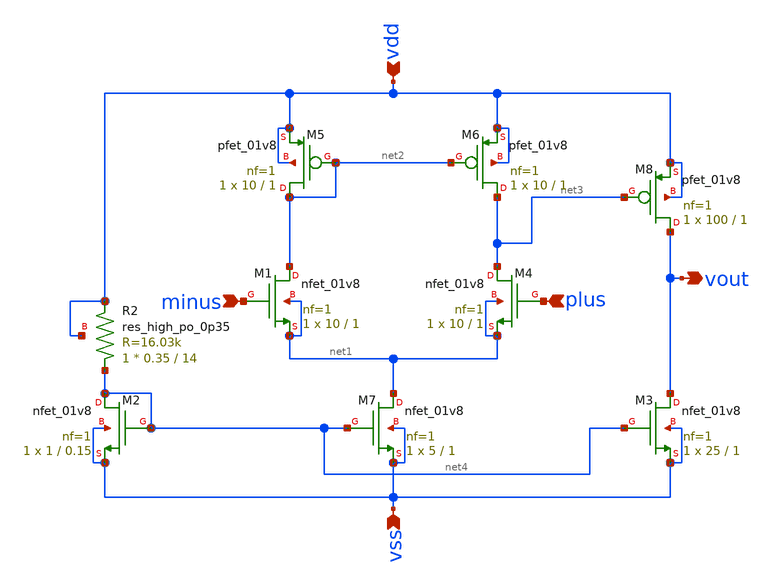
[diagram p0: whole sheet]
** sch_path: analog/schematics/bootcamp_opamp.sch
**.subckt bootcamp_opamp vdd minus plus vss vout
*.ipin vdd
*.ipin minus
*.ipin plus
*.ipin vss
*.opin vout
XM1 net2 minus net1 net1 sky130_fd_pr__nfet_01v8 L=1 W=10 nf=1 ad='int((nf+1)/2) * W/nf * 0.29' as='int((nf+2)/2) * W/nf * 0.29'
+ pd='2*int((nf+1)/2) * (W/nf + 0.29)' ps='2*int((nf+2)/2) * (W/nf + 0.29)' nrd='0.29 / W' nrs='0.29 / W'
+ sa=0 sb=0 sd=0 mult=1 m=1
XM4 net3 plus net1 net1 sky130_fd_pr__nfet_01v8 L=1 W=10 nf=1 ad='int((nf+1)/2) * W/nf * 0.29' as='int((nf+2)/2) * W/nf * 0.29'
+ pd='2*int((nf+1)/2) * (W/nf + 0.29)' ps='2*int((nf+2)/2) * (W/nf + 0.29)' nrd='0.29 / W' nrs='0.29 / W'
+ sa=0 sb=0 sd=0 mult=1 m=1
XM5 net2 net2 vdd vdd sky130_fd_pr__pfet_01v8 L=1 W=10 nf=1 ad='int((nf+1)/2) * W/nf * 0.29' as='int((nf+2)/2) * W/nf * 0.29'
+ pd='2*int((nf+1)/2) * (W/nf + 0.29)' ps='2*int((nf+2)/2) * (W/nf + 0.29)' nrd='0.29 / W' nrs='0.29 / W'
+ sa=0 sb=0 sd=0 mult=1 m=1
XM6 net3 net2 vdd vdd sky130_fd_pr__pfet_01v8 L=1 W=10 nf=1 ad='int((nf+1)/2) * W/nf * 0.29' as='int((nf+2)/2) * W/nf * 0.29'
+ pd='2*int((nf+1)/2) * (W/nf + 0.29)' ps='2*int((nf+2)/2) * (W/nf + 0.29)' nrd='0.29 / W' nrs='0.29 / W'
+ sa=0 sb=0 sd=0 mult=1 m=1
XM2 net4 net4 vss vss sky130_fd_pr__nfet_01v8 L=0.15 W=1 nf=1 ad='int((nf+1)/2) * W/nf * 0.29' as='int((nf+2)/2) * W/nf * 0.29'
+ pd='2*int((nf+1)/2) * (W/nf + 0.29)' ps='2*int((nf+2)/2) * (W/nf + 0.29)' nrd='0.29 / W' nrs='0.29 / W'
+ sa=0 sb=0 sd=0 mult=1 m=1
XM7 net1 net4 vss vss sky130_fd_pr__nfet_01v8 L=1 W=5 nf=1 ad='int((nf+1)/2) * W/nf * 0.29' as='int((nf+2)/2) * W/nf * 0.29'
+ pd='2*int((nf+1)/2) * (W/nf + 0.29)' ps='2*int((nf+2)/2) * (W/nf + 0.29)' nrd='0.29 / W' nrs='0.29 / W'
+ sa=0 sb=0 sd=0 mult=1 m=1
XM3 vout net4 vss vss sky130_fd_pr__nfet_01v8 L=1 W=25 nf=1 ad='int((nf+1)/2) * W/nf * 0.29' as='int((nf+2)/2) * W/nf * 0.29'
+ pd='2*int((nf+1)/2) * (W/nf + 0.29)' ps='2*int((nf+2)/2) * (W/nf + 0.29)' nrd='0.29 / W' nrs='0.29 / W'
+ sa=0 sb=0 sd=0 mult=1 m=1
XM8 vout net3 vdd vdd sky130_fd_pr__pfet_01v8 L=1 W=100 nf=1 ad='int((nf+1)/2) * W/nf * 0.29' as='int((nf+2)/2) * W/nf * 0.29'
+ pd='2*int((nf+1)/2) * (W/nf + 0.29)' ps='2*int((nf+2)/2) * (W/nf + 0.29)' nrd='0.29 / W' nrs='0.29 / W'
+ sa=0 sb=0 sd=0 mult=1 m=1
XR2 net4 vdd vdd sky130_fd_pr__res_high_po_0p35 L=14 mult=1 m=1
**.ends
.end
